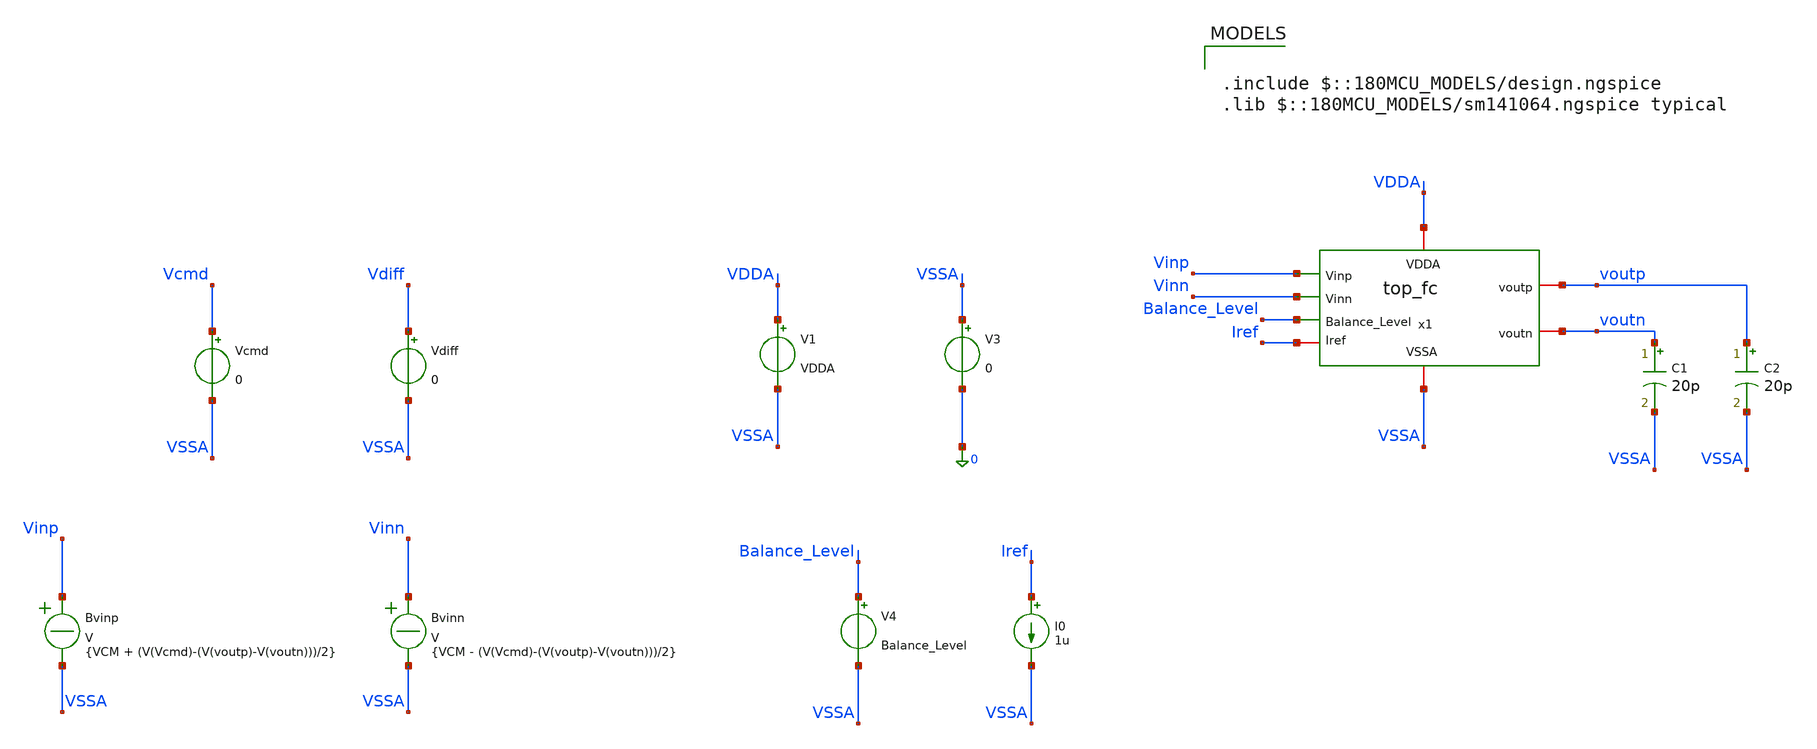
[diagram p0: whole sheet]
** sch_path: Folded_cascode/testbenches/top_fc_output_swing_tb.sch
**.subckt top_fc_output_swing_tb
x1 Balance_Level Vinp voutp VDDA voutn Vinn Iref VSSA top_fc
C1 voutn VSSA 20p m=1
C2 voutp VSSA 20p m=1
V1 VDDA VSSA VDDA
V3 VSSA 0 0
V4 Balance_Level VSSA Balance_Level
I0 Iref VSSA 1u
Bvinp Vinp VSSA V = {VCM + (V(Vcmd)-(V(voutp)-V(voutn)))/2}
Bvinn Vinn VSSA V = {VCM - (V(Vcmd)-(V(voutp)-V(voutn)))/2}
Vdiff Vdiff VSSA 0
Vcmd Vcmd VSSA 0
**** begin user architecture code

.include $::180MCU_MODELS/design.ngspice
.lib $::180MCU_MODELS/sm141064.ngspice typical



.temp 27
.param VDDA = 5
.param Balance_Level = 1.5
.param VD = 0
.param VCM = 2.5

.control
option sparse
set filetype=ascii
set wr_singlescale
set wr_vecnames
save all
save @m.x1.x1.xm1.m0[id]
save @m.x1.x1.xm1.m0[gm]
save @m.x1.x1.xm1.m0[vgs]
save @m.x1.x1.xm1.m0[vds]
save @m.x1.x1.xm1.m0[vth]
save @m.x1.x1.xm1.m0[gds]
save @m.x1.x1.xm1.m0[vdsat]

save @m.x1.x1.xm2.m0[id]
save @m.x1.x1.xm2.m0[gm]
save @m.x1.x1.xm2.m0[vgs]
save @m.x1.x1.xm2.m0[vds]
save @m.x1.x1.xm2.m0[vth]
save @m.x1.x1.xm2.m0[gds]
save @m.x1.x1.xm2.m0[vdsat]

save @m.x1.x1.xm9.m0[id]
save @m.x1.x1.xm9.m0[gm]
save @m.x1.x1.xm9.m0[vgs]
save @m.x1.x1.xm9.m0[vds]
save @m.x1.x1.xm9.m0[vth]
save @m.x1.x1.xm9.m0[gds]
save @m.x1.x1.xm9.m0[vdsat]

save @m.x1.x1.xm8.m0[id]
save @m.x1.x1.xm8.m0[gm]
save @m.x1.x1.xm8.m0[vgs]
save @m.x1.x1.xm8.m0[vds]
save @m.x1.x1.xm8.m0[vth]
save @m.x1.x1.xm8.m0[gds]
save @m.x1.x1.xm8.m0[vdsat]

save @m.x1.x1.xm6.m0[id]
save @m.x1.x1.xm6.m0[gm]
save @m.x1.x1.xm6.m0[vgs]
save @m.x1.x1.xm6.m0[vds]
save @m.x1.x1.xm6.m0[vth]
save @m.x1.x1.xm6.m0[gds]
save @m.x1.x1.xm6.m0[vdsat]

save @m.x1.x1.xm5.m0[id]
save @m.x1.x1.xm5.m0[gm]
save @m.x1.x1.xm5.m0[vgs]
save @m.x1.x1.xm5.m0[vds]
save @m.x1.x1.xm5.m0[vth]
save @m.x1.x1.xm5.m0[gds]
save @m.x1.x1.xm5.m0[vdsat]

save @m.x1.x2.xm1.m0[id]
save @m.x1.x2.xm1.m0[gm]
save @m.x1.x2.xm1.m0[vgs]
save @m.x1.x2.xm1.m0[vds]
save @m.x1.x2.xm1.m0[vth]
save @m.x1.x2.xm1.m0[gds]

save @m.x1.x2.xm2.m0[id]
save @m.x1.x2.xm2.m0[gm]
save @m.x1.x2.xm2.m0[vgs]
save @m.x1.x2.xm2.m0[vds]
save @m.x1.x2.xm2.m0[vth]
save @m.x1.x2.xm2.m0[gds]

save @m.x1.x2.xm3.m0[id]
save @m.x1.x2.xm3.m0[gm]
save @m.x1.x2.xm3.m0[vgs]
save @m.x1.x2.xm3.m0[vds]
save @m.x1.x2.xm3.m0[vth]
save @m.x1.x2.xm3.m0[gds]

save @m.x1.x2.xm4.m0[id]
save @m.x1.x2.xm4.m0[gm]
save @m.x1.x2.xm4.m0[vgs]
save @m.x1.x2.xm4.m0[vds]
save @m.x1.x2.xm4.m0[vth]
save @m.x1.x2.xm4.m0[gds]

save @m.x1.x2.xm5.m0[id]
save @m.x1.x2.xm5.m0[gm]
save @m.x1.x2.xm5.m0[vgs]
save @m.x1.x2.xm5.m0[vds]
save @m.x1.x2.xm5.m0[vth]
save @m.x1.x2.xm5.m0[gds]

save @m.x1.x2.xm6.m0[id]
save @m.x1.x2.xm6.m0[gm]
save @m.x1.x2.xm6.m0[vgs]
save @m.x1.x2.xm6.m0[vds]
save @m.x1.x2.xm6.m0[vth]
save @m.x1.x2.xm6.m0[gds]

save @m.x1.x2.xm7.m0[id]
save @m.x1.x2.xm7.m0[gm]
save @m.x1.x2.xm7.m0[vgs]
save @m.x1.x2.xm7.m0[vds]
save @m.x1.x2.xm7.m0[vth]
save @m.x1.x2.xm7.m0[gds]

save @m.x1.x2.xm8.m0[id]
save @m.x1.x2.xm8.m0[gm]
save @m.x1.x2.xm8.m0[vgs]
save @m.x1.x2.xm8.m0[vds]
save @m.x1.x2.xm8.m0[vth]
save @m.x1.x2.xm8.m0[gds]

save @m.x1.x2.xm9.m0[id]
save @m.x1.x2.xm9.m0[gm]
save @m.x1.x2.xm9.m0[vgs]
save @m.x1.x2.xm9.m0[vds]
save @m.x1.x2.xm9.m0[vth]
save @m.x1.x2.xm9.m0[gds]

save @m.x1.x3.xm1.m0[id]
save @m.x1.x3.xm1.m0[gm]
save @m.x1.x3.xm1.m0[vgs]
save @m.x1.x3.xm1.m0[vds]
save @m.x1.x3.xm1.m0[vth]
save @m.x1.x3.xm1.m0[gds]

save @m.x1.x3.xm2.m0[id]
save @m.x1.x3.xm2.m0[gm]
save @m.x1.x3.xm2.m0[vgs]
save @m.x1.x3.xm2.m0[vds]
save @m.x1.x3.xm2.m0[vth]
save @m.x1.x3.xm2.m0[gds]

save @m.x1.x3.xm3.m0[id]
save @m.x1.x3.xm3.m0[gm]
save @m.x1.x3.xm3.m0[vgs]
save @m.x1.x3.xm3.m0[vds]
save @m.x1.x3.xm3.m0[vth]
save @m.x1.x3.xm3.m0[gds]

save @m.x1.x3.xm4.m0[id]
save @m.x1.x3.xm4.m0[gm]
save @m.x1.x3.xm4.m0[vgs]
save @m.x1.x3.xm4.m0[vds]
save @m.x1.x3.xm4.m0[vth]
save @m.x1.x3.xm4.m0[gds]

save @m.x1.x3.xm5.m0[id]
save @m.x1.x3.xm5.m0[gm]
save @m.x1.x3.xm5.m0[vgs]
save @m.x1.x3.xm5.m0[vds]
save @m.x1.x3.xm5.m0[vth]
save @m.x1.x3.xm5.m0[gds]

save @m.x1.x3.xm6.m0[id]
save @m.x1.x3.xm6.m0[gm]
save @m.x1.x3.xm6.m0[vgs]
save @m.x1.x3.xm6.m0[vds]
save @m.x1.x3.xm6.m0[vth]
save @m.x1.x3.xm6.m0[gds]

save @m.x1.x3.xm7.m0[id]
save @m.x1.x3.xm7.m0[gm]
save @m.x1.x3.xm7.m0[vgs]
save @m.x1.x3.xm7.m0[vds]
save @m.x1.x3.xm7.m0[vth]
save @m.x1.x3.xm7.m0[gds]

save @m.x1.x3.xm8.m0[id]
save @m.x1.x3.xm8.m0[gm]
save @m.x1.x3.xm8.m0[vgs]
save @m.x1.x3.xm8.m0[vds]
save @m.x1.x3.xm8.m0[vth]
save @m.x1.x3.xm8.m0[gds]

save @m.x1.x3.xm9.m0[id]
save @m.x1.x3.xm9.m0[gm]
save @m.x1.x3.xm9.m0[vgs]
save @m.x1.x3.xm9.m0[vds]
save @m.x1.x3.xm9.m0[vth]
save @m.x1.x3.xm9.m0[gds]

save @m.x1.x3.xm10.m0[id]
save @m.x1.x3.xm10.m0[gm]
save @m.x1.x3.xm10.m0[vgs]
save @m.x1.x3.xm10.m0[vds]
save @m.x1.x3.xm10.m0[vth]
save @m.x1.x3.xm10.m0[gds]

save @m.x1.x3.xm11.m0[id]
save @m.x1.x3.xm11.m0[gm]
save @m.x1.x3.xm11.m0[vgs]
save @m.x1.x3.xm11.m0[vds]
save @m.x1.x3.xm11.m0[vth]
save @m.x1.x3.xm11.m0[gds]

save @m.x1.x3.xm12.m0[id]
save @m.x1.x3.xm12.m0[gm]
save @m.x1.x3.xm12.m0[vgs]
save @m.x1.x3.xm12.m0[vds]
save @m.x1.x3.xm12.m0[vth]
save @m.x1.x3.xm12.m0[gds]

save @m.x1.x3.xm13.m0[id]
save @m.x1.x3.xm13.m0[gm]
save @m.x1.x3.xm13.m0[vgs]
save @m.x1.x3.xm13.m0[vds]
save @m.x1.x3.xm13.m0[vth]
save @m.x1.x3.xm13.m0[gds]

save @m.x1.x3.xm14.m0[id]
save @m.x1.x3.xm14.m0[gm]
save @m.x1.x3.xm14.m0[vgs]
save @m.x1.x3.xm14.m0[vds]
save @m.x1.x3.xm14.m0[vth]
save @m.x1.x3.xm14.m0[gds]

save @m.x1.x3.xm15.m0[id]
save @m.x1.x3.xm15.m0[gm]
save @m.x1.x3.xm15.m0[vgs]
save @m.x1.x3.xm15.m0[vds]
save @m.x1.x3.xm15.m0[vth]
save @m.x1.x3.xm15.m0[gds]

save @m.x1.x3.xm16.m0[id]
save @m.x1.x3.xm16.m0[gm]
save @m.x1.x3.xm16.m0[vgs]
save @m.x1.x3.xm16.m0[vds]
save @m.x1.x3.xm16.m0[vth]
save @m.x1.x3.xm16.m0[gds]

save @m.x1.x3.xm17.m0[id]
save @m.x1.x3.xm17.m0[gm]
save @m.x1.x3.xm17.m0[vgs]
save @m.x1.x3.xm17.m0[vds]
save @m.x1.x3.xm17.m0[vth]
save @m.x1.x3.xm17.m0[gds]

save @m.x1.x3.xm18.m0[id]
save @m.x1.x3.xm18.m0[gm]
save @m.x1.x3.xm18.m0[vgs]
save @m.x1.x3.xm18.m0[vds]
save @m.x1.x3.xm18.m0[vth]
save @m.x1.x3.xm18.m0[gds]

save @m.x1.x3.xm21.m0[id]
save @m.x1.x3.xm21.m0[gm]
save @m.x1.x3.xm21.m0[vgs]
save @m.x1.x3.xm21.m0[vds]
save @m.x1.x3.xm21.m0[vth]
save @m.x1.x3.xm21.m0[gds]

save @m.x1.x3.xm22.m0[id]
save @m.x1.x3.xm22.m0[gm]
save @m.x1.x3.xm22.m0[vgs]
save @m.x1.x3.xm22.m0[vds]
save @m.x1.x3.xm22.m0[vth]
save @m.x1.x3.xm22.m0[gds]

op
write top_fc_op_tb.raw all

* ============================================================
* SAVE OUTPUT DEVICE OPERATING POINT PARAMETERS
* ============================================================

save @m.x1.x1.xm6.m0[vds]
save @m.x1.x1.xm6.m0[vdsat]

save @m.x1.x1.xm7.m0[vds]
save @m.x1.x1.xm7.m0[vdsat]

save @m.x1.x1.xm8.m0[vds]
save @m.x1.x1.xm8.m0[vdsat]

save @m.x1.x1.xm10.m0[vds]
save @m.x1.x1.xm10.m0[vdsat]

* ============================================================
* DC SWEEP
*
* Command differential output from -4.5 V to +4.5 V
* ============================================================

dc Vcmd -4.5 4.5 5m


* ============================================================
* OUTPUT QUANTITIES
* ============================================================

let vod = v(voutp)-v(voutn)
let vocm = (v(voutp)+v(voutn))/2

let tracking_error = vod-v(Vcmd)


* ============================================================
* SATURATION MARGINS
*
* margin > 0 : saturation
* margin = 0 : saturation boundary
* margin < 0 : outside saturation
* ============================================================

let sat_xm6 = abs(@m.x1.x1.xm6.m0[vds])-abs(@m.x1.x1.xm6.m0[vdsat])
let sat_xm7 = abs(@m.x1.x1.xm7.m0[vds])-abs(@m.x1.x1.xm7.m0[vdsat])

let sat_xm8 = abs(@m.x1.x1.xm8.m0[vds])-abs(@m.x1.x1.xm8.m0[vdsat])
let sat_xm10 = abs(@m.x1.x1.xm10.m0[vds])-abs(@m.x1.x1.xm10.m0[vdsat])


* ============================================================
* RAW EXTREMA
* ============================================================

meas dc voutp_min MIN v(voutp)
meas dc voutp_max MAX v(voutp)

meas dc voutn_min MIN v(voutn)
meas dc voutn_max MAX v(voutn)

meas dc vod_min MIN vod
meas dc vod_max MAX vod

meas dc vocm_min MIN vocm
meas dc vocm_max MAX vocm


let voutp_pp = voutp_max-voutp_min
let voutn_pp = voutn_max-voutn_min
let vod_pp = vod_max-vod_min


* ============================================================
* PRINT RESULTS
* ============================================================

print voutp_min
print voutp_max
print voutp_pp

print voutn_min
print voutn_max
print voutn_pp

print vod_min
print vod_max
print vod_pp

print vocm_min
print vocm_max


* ============================================================
* SAVE RAW FILE
* ============================================================

write top_fc_output_swing_tb.raw


* ============================================================
* EXPORT DATA
*
* ngspice wrdata automatically writes the sweep variable
* as the first column.
*
* Columns will therefore contain:
*
* Vcmd
* Voutp
* Voutn
* Vod
* Vocm
* tracking_error
* sat_xm6
* sat_xm7
* sat_xm8
* sat_xm10
* ============================================================

wrdata output_swing.dat v(voutp) v(voutn) vod vocm tracking_error sat_xm6 sat_xm7 sat_xm8 sat_xm10


* ============================================================
* PLOTS
* ============================================================

* Actual differential output versus command
plot vod v(Vcmd)

* Tracking error
plot tracking_error

* Single-ended outputs
plot v(voutp) v(voutn)

* Output common-mode
plot vocm

* NMOS output-device saturation margins
plot sat_xm6 sat_xm7

* PMOS output-device saturation margins
plot sat_xm8 sat_xm10

.endc


**** end user architecture code
**.ends
.end
